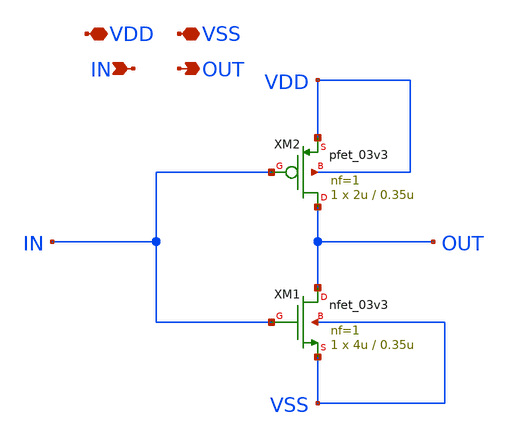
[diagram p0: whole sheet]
** sch_path: Clock_Generator_PAKISTAN_02/Schematics/GF_INV_PFD.sch
**.subckt GF_INV_PFD VDD VSS IN OUT
*.iopin VDD
*.iopin VSS
*.ipin IN
*.opin OUT
XM1 OUT IN VSS VSS nfet_03v3 L=0.35u W=4u nf=1 ad='int((nf+1)/2) * W/nf * 0.18u' as='int((nf+2)/2) * W/nf * 0.18u'
+ pd='2*int((nf+1)/2) * (W/nf + 0.18u)' ps='2*int((nf+2)/2) * (W/nf + 0.18u)' nrd='0.18u / W' nrs='0.18u / W'
+ sa=0 sb=0 sd=0 m=1
XM2 OUT IN VDD VDD pfet_03v3 L=0.35u W=2u nf=1 ad='int((nf+1)/2) * W/nf * 0.18u' as='int((nf+2)/2) * W/nf * 0.18u'
+ pd='2*int((nf+1)/2) * (W/nf + 0.18u)' ps='2*int((nf+2)/2) * (W/nf + 0.18u)' nrd='0.18u / W' nrs='0.18u / W'
+ sa=0 sb=0 sd=0 m=1
**.ends
.end
